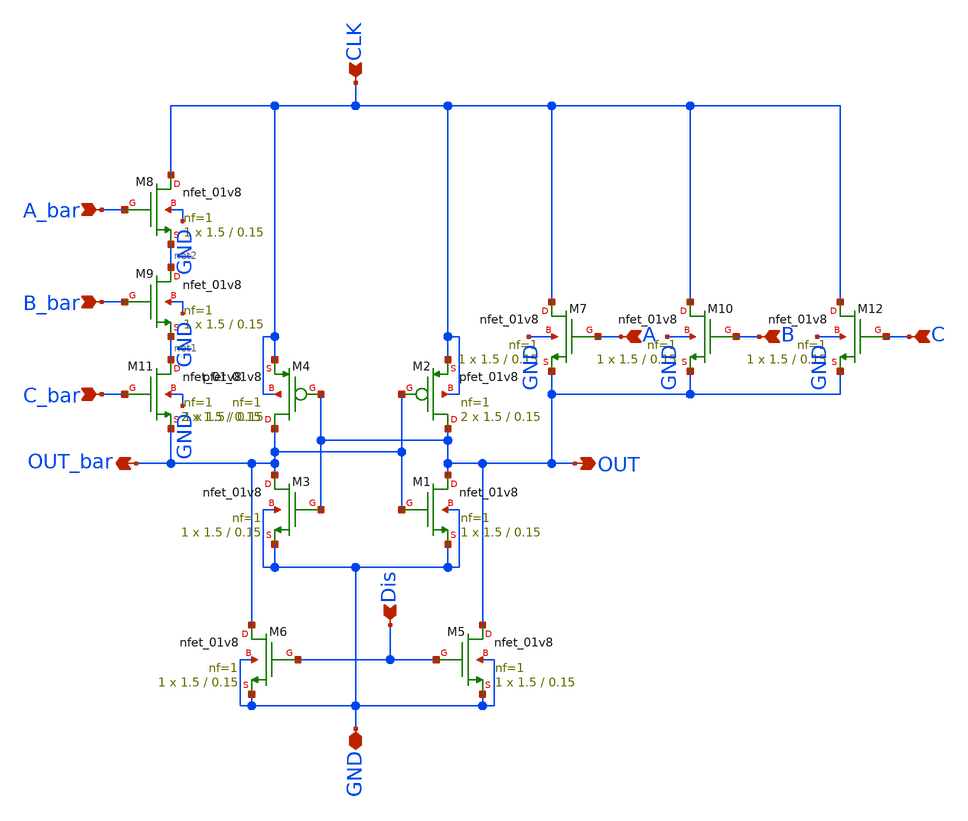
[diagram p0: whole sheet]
** sch_path: skywater_stuff/EESPFAL_3in_NOR.sch
**.subckt EESPFAL_3in_NOR A A_bar B B_bar C C_bar OUT OUT_bar Dis GND CLK GND
*.ipin A
*.ipin A_bar
*.ipin B
*.ipin B_bar
*.ipin C
*.ipin C_bar
*.opin OUT
*.opin OUT_bar
*.ipin Dis
*.iopin GND
*.ipin CLK
*.iopin GND
XM9 net2 B_bar net1 GND sky130_fd_pr__nfet_01v8 L=0.15 W=1.5 nf=1 ad='int((nf+1)/2) * W/nf * 0.29' as='int((nf+2)/2) * W/nf * 0.29'
+ pd='2*int((nf+1)/2) * (W/nf + 0.29)' ps='2*int((nf+2)/2) * (W/nf + 0.29)' nrd='0.29 / W' nrs='0.29 / W'
+ sa=0 sb=0 sd=0 mult=1 m=1
XM4 OUT_bar OUT CLK CLK sky130_fd_pr__pfet_01v8 L=0.15 W=1.5 nf=1 ad='int((nf+1)/2) * W/nf * 0.29' as='int((nf+2)/2) * W/nf * 0.29'
+ pd='2*int((nf+1)/2) * (W/nf + 0.29)' ps='2*int((nf+2)/2) * (W/nf + 0.29)' nrd='0.29 / W' nrs='0.29 / W'
+ sa=0 sb=0 sd=0 mult=2 m=2
XM10 CLK B OUT GND sky130_fd_pr__nfet_01v8 L=0.15 W=1.5 nf=1 ad='int((nf+1)/2) * W/nf * 0.29' as='int((nf+2)/2) * W/nf * 0.29'
+ pd='2*int((nf+1)/2) * (W/nf + 0.29)' ps='2*int((nf+2)/2) * (W/nf + 0.29)' nrd='0.29 / W' nrs='0.29 / W'
+ sa=0 sb=0 sd=0 mult=1 m=1
XM3 OUT_bar OUT GND GND sky130_fd_pr__nfet_01v8 L=0.15 W=1.5 nf=1 ad='int((nf+1)/2) * W/nf * 0.29' as='int((nf+2)/2) * W/nf * 0.29'
+ pd='2*int((nf+1)/2) * (W/nf + 0.29)' ps='2*int((nf+2)/2) * (W/nf + 0.29)' nrd='0.29 / W' nrs='0.29 / W'
+ sa=0 sb=0 sd=0 mult=1 m=1
XM8 CLK A_bar net2 GND sky130_fd_pr__nfet_01v8 L=0.15 W=1.5 nf=1 ad='int((nf+1)/2) * W/nf * 0.29' as='int((nf+2)/2) * W/nf * 0.29'
+ pd='2*int((nf+1)/2) * (W/nf + 0.29)' ps='2*int((nf+2)/2) * (W/nf + 0.29)' nrd='0.29 / W' nrs='0.29 / W'
+ sa=0 sb=0 sd=0 mult=1 m=1
XM1 OUT OUT_bar GND GND sky130_fd_pr__nfet_01v8 L=0.15 W=1.5 nf=1 ad='int((nf+1)/2) * W/nf * 0.29' as='int((nf+2)/2) * W/nf * 0.29'
+ pd='2*int((nf+1)/2) * (W/nf + 0.29)' ps='2*int((nf+2)/2) * (W/nf + 0.29)' nrd='0.29 / W' nrs='0.29 / W'
+ sa=0 sb=0 sd=0 mult=1 m=1
XM7 CLK A OUT GND sky130_fd_pr__nfet_01v8 L=0.15 W=1.5 nf=1 ad='int((nf+1)/2) * W/nf * 0.29' as='int((nf+2)/2) * W/nf * 0.29'
+ pd='2*int((nf+1)/2) * (W/nf + 0.29)' ps='2*int((nf+2)/2) * (W/nf + 0.29)' nrd='0.29 / W' nrs='0.29 / W'
+ sa=0 sb=0 sd=0 mult=1 m=1
XM2 OUT OUT_bar CLK CLK sky130_fd_pr__pfet_01v8 L=0.15 W=1.5 nf=1 ad='int((nf+1)/2) * W/nf * 0.29' as='int((nf+2)/2) * W/nf * 0.29'
+ pd='2*int((nf+1)/2) * (W/nf + 0.29)' ps='2*int((nf+2)/2) * (W/nf + 0.29)' nrd='0.29 / W' nrs='0.29 / W'
+ sa=0 sb=0 sd=0 mult=2 m=2
XM5 OUT Dis GND GND sky130_fd_pr__nfet_01v8 L=0.15 W=1.5 nf=1 ad='int((nf+1)/2) * W/nf * 0.29' as='int((nf+2)/2) * W/nf * 0.29'
+ pd='2*int((nf+1)/2) * (W/nf + 0.29)' ps='2*int((nf+2)/2) * (W/nf + 0.29)' nrd='0.29 / W' nrs='0.29 / W'
+ sa=0 sb=0 sd=0 mult=1 m=1
XM11 net1 C_bar OUT_bar GND sky130_fd_pr__nfet_01v8 L=0.15 W=1.5 nf=1 ad='int((nf+1)/2) * W/nf * 0.29'
+ as='int((nf+2)/2) * W/nf * 0.29' pd='2*int((nf+1)/2) * (W/nf + 0.29)' ps='2*int((nf+2)/2) * (W/nf + 0.29)'
+ nrd='0.29 / W' nrs='0.29 / W' sa=0 sb=0 sd=0 mult=1 m=1
XM6 OUT_bar Dis GND GND sky130_fd_pr__nfet_01v8 L=0.15 W=1.5 nf=1 ad='int((nf+1)/2) * W/nf * 0.29' as='int((nf+2)/2) * W/nf * 0.29'
+ pd='2*int((nf+1)/2) * (W/nf + 0.29)' ps='2*int((nf+2)/2) * (W/nf + 0.29)' nrd='0.29 / W' nrs='0.29 / W'
+ sa=0 sb=0 sd=0 mult=1 m=1
XM12 CLK C OUT GND sky130_fd_pr__nfet_01v8 L=0.15 W=1.5 nf=1 ad='int((nf+1)/2) * W/nf * 0.29' as='int((nf+2)/2) * W/nf * 0.29'
+ pd='2*int((nf+1)/2) * (W/nf + 0.29)' ps='2*int((nf+2)/2) * (W/nf + 0.29)' nrd='0.29 / W' nrs='0.29 / W'
+ sa=0 sb=0 sd=0 mult=1 m=1
**.ends
.end
